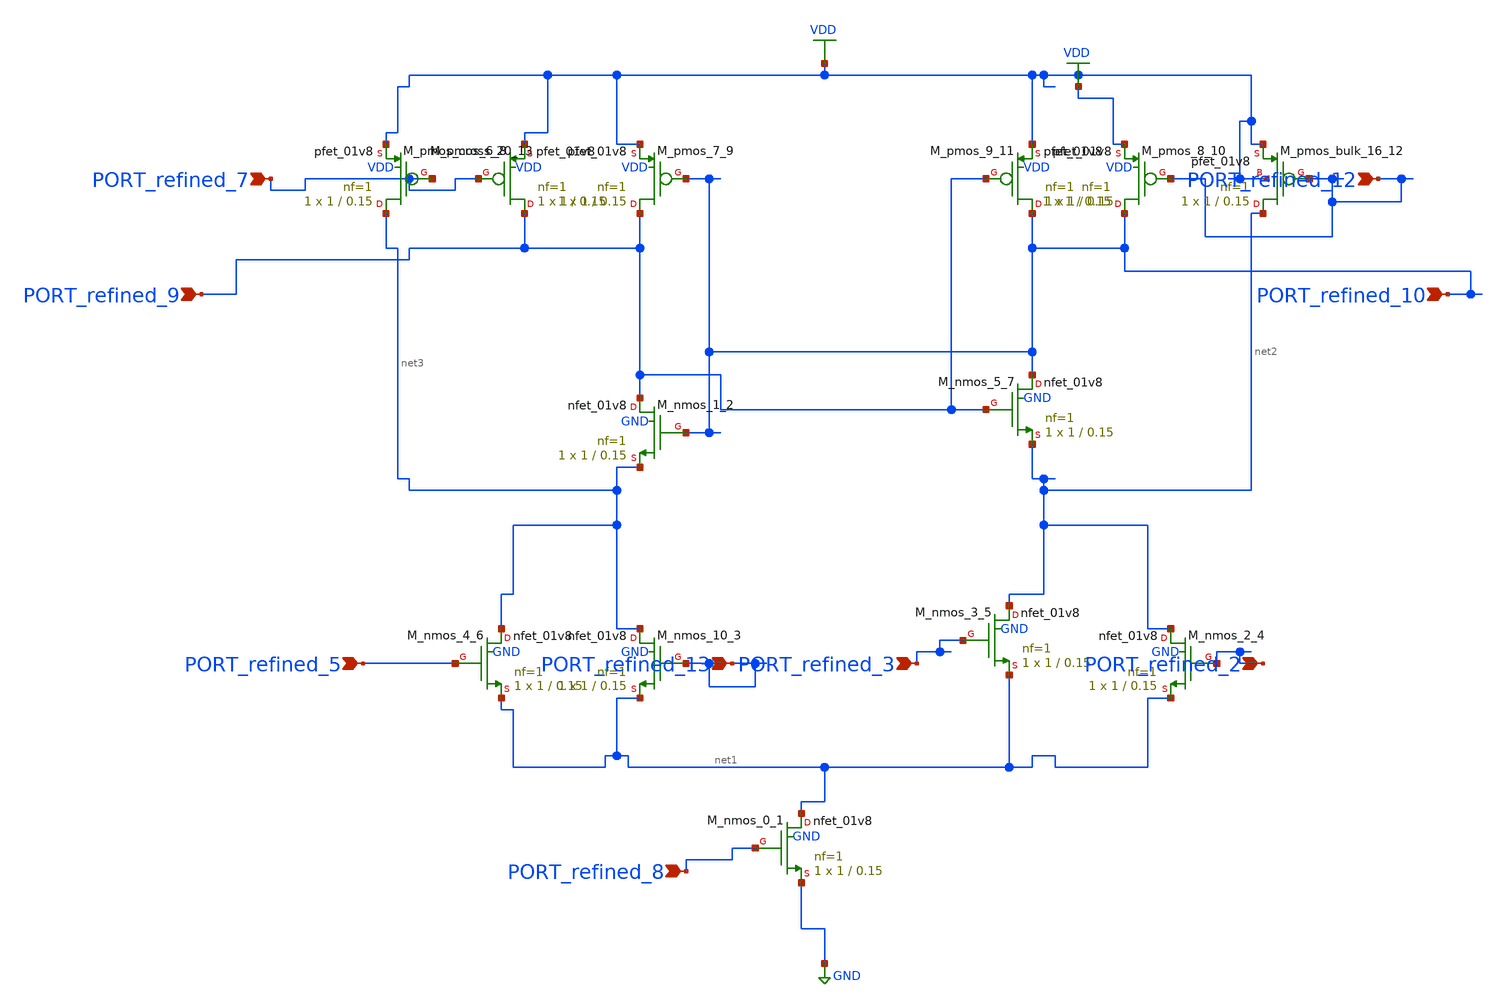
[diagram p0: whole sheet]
** sch_path: schematics/Image2Net/038.sch
**.subckt 038 PORT_refined_9 PORT_refined_10 PORT_refined_5 PORT_refined_2 PORT_refined_3
*+ PORT_refined_8 PORT_refined_7 PORT_refined_13 PORT_refined_12
*.ipin PORT_refined_9
*.ipin PORT_refined_10
*.ipin PORT_refined_5
*.ipin PORT_refined_2
*.ipin PORT_refined_3
*.ipin PORT_refined_8
*.ipin PORT_refined_7
*.ipin PORT_refined_13
*.ipin PORT_refined_12
XM_nmos_0_1 net1 PORT_refined_8 GND GND sky130_fd_pr__nfet_01v8 L=0.15 W=1 nf=1 ad='int((1 + 1)/2) * 1 / 1 * 0.29'
+ as='int((1 + 2)/2) * 1 / 1 * 0.29' pd='2*int((1 + 1)/2) * (1 / 1 + 0.29)' ps='2*int((1 + 2)/2) * (1 / 1 + 0.29)'
+ nrd='0.29 / 1 ' nrs='0.29 / 1 ' sa=0 sb=0 sd=0 mult=1 m=1
XM_nmos_1_2 PORT_refined_9 PORT_refined_10 net3 GND sky130_fd_pr__nfet_01v8 L=0.15 W=1 nf=1 ad='int((1 + 1)/2) * 1 / 1 * 0.29'
+ as='int((1 + 2)/2) * 1 / 1 * 0.29' pd='2*int((1 + 1)/2) * (1 / 1 + 0.29)' ps='2*int((1 + 2)/2) * (1 / 1 + 0.29)'
+ nrd='0.29 / 1 ' nrs='0.29 / 1 ' sa=0 sb=0 sd=0 mult=1 m=1
XM_nmos_10_3 net3 PORT_refined_13 net1 GND sky130_fd_pr__nfet_01v8 L=0.15 W=1 nf=1 ad='int((1 + 1)/2) * 1 / 1 * 0.29'
+ as='int((1 + 2)/2) * 1 / 1 * 0.29' pd='2*int((1 + 1)/2) * (1 / 1 + 0.29)' ps='2*int((1 + 2)/2) * (1 / 1 + 0.29)'
+ nrd='0.29 / 1 ' nrs='0.29 / 1 ' sa=0 sb=0 sd=0 mult=1 m=1
XM_nmos_2_4 net2 PORT_refined_2 net1 GND sky130_fd_pr__nfet_01v8 L=0.15 W=1 nf=1 ad='int((1 + 1)/2) * 1 / 1 * 0.29'
+ as='int((1 + 2)/2) * 1 / 1 * 0.29' pd='2*int((1 + 1)/2) * (1 / 1 + 0.29)' ps='2*int((1 + 2)/2) * (1 / 1 + 0.29)'
+ nrd='0.29 / 1 ' nrs='0.29 / 1 ' sa=0 sb=0 sd=0 mult=1 m=1
XM_nmos_3_5 net2 PORT_refined_3 net1 GND sky130_fd_pr__nfet_01v8 L=0.15 W=1 nf=1 ad='int((1 + 1)/2) * 1 / 1 * 0.29'
+ as='int((1 + 2)/2) * 1 / 1 * 0.29' pd='2*int((1 + 1)/2) * (1 / 1 + 0.29)' ps='2*int((1 + 2)/2) * (1 / 1 + 0.29)'
+ nrd='0.29 / 1 ' nrs='0.29 / 1 ' sa=0 sb=0 sd=0 mult=1 m=1
XM_nmos_4_6 net3 PORT_refined_5 net1 GND sky130_fd_pr__nfet_01v8 L=0.15 W=1 nf=1 ad='int((1 + 1)/2) * 1 / 1 * 0.29'
+ as='int((1 + 2)/2) * 1 / 1 * 0.29' pd='2*int((1 + 1)/2) * (1 / 1 + 0.29)' ps='2*int((1 + 2)/2) * (1 / 1 + 0.29)'
+ nrd='0.29 / 1 ' nrs='0.29 / 1 ' sa=0 sb=0 sd=0 mult=1 m=1
XM_nmos_5_7 PORT_refined_10 PORT_refined_9 net2 GND sky130_fd_pr__nfet_01v8 L=0.15 W=1 nf=1 ad='int((1 + 1)/2) * 1 / 1 * 0.29'
+ as='int((1 + 2)/2) * 1 / 1 * 0.29' pd='2*int((1 + 1)/2) * (1 / 1 + 0.29)' ps='2*int((1 + 2)/2) * (1 / 1 + 0.29)'
+ nrd='0.29 / 1 ' nrs='0.29 / 1 ' sa=0 sb=0 sd=0 mult=1 m=1
XM_pmos_6_8 PORT_refined_9 PORT_refined_7 VDD VDD sky130_fd_pr__pfet_01v8 L=0.15 W=1 nf=1 ad='int((1 + 1)/2) * 1 / 1 * 0.29'
+ as='int((1 + 2)/2) * 1 / 1 * 0.29' pd='2*int((1 + 1)/2) * (1 / 1 + 0.29)' ps='2*int((1 + 2)/2) * (1 / 1 + 0.29)'
+ nrd='0.29 / 1 ' nrs='0.29 / 1 ' sa=0 sb=0 sd=0 mult=1 m=1
XM_pmos_7_9 PORT_refined_9 PORT_refined_10 VDD VDD sky130_fd_pr__pfet_01v8 L=0.15 W=1 nf=1 ad='int((1 + 1)/2) * 1 / 1 * 0.29'
+ as='int((1 + 2)/2) * 1 / 1 * 0.29' pd='2*int((1 + 1)/2) * (1 / 1 + 0.29)' ps='2*int((1 + 2)/2) * (1 / 1 + 0.29)'
+ nrd='0.29 / 1 ' nrs='0.29 / 1 ' sa=0 sb=0 sd=0 mult=1 m=1
XM_pmos_8_10 PORT_refined_10 PORT_refined_12 VDD VDD sky130_fd_pr__pfet_01v8 L=0.15 W=1 nf=1 ad='int((1 + 1)/2) * 1 / 1 * 0.29'
+ as='int((1 + 2)/2) * 1 / 1 * 0.29' pd='2*int((1 + 1)/2) * (1 / 1 + 0.29)' ps='2*int((1 + 2)/2) * (1 / 1 + 0.29)'
+ nrd='0.29 / 1 ' nrs='0.29 / 1 ' sa=0 sb=0 sd=0 mult=1 m=1
XM_pmos_9_11 PORT_refined_10 PORT_refined_9 VDD VDD sky130_fd_pr__pfet_01v8 L=0.15 W=1 nf=1 ad='int((1 + 1)/2) * 1 / 1 * 0.29'
+ as='int((1 + 2)/2) * 1 / 1 * 0.29' pd='2*int((1 + 1)/2) * (1 / 1 + 0.29)' ps='2*int((1 + 2)/2) * (1 / 1 + 0.29)'
+ nrd='0.29 / 1 ' nrs='0.29 / 1 ' sa=0 sb=0 sd=0 mult=1 m=1
XM_pmos_bulk_16_12 net2 PORT_refined_12 VDD VDD sky130_fd_pr__pfet_01v8 L=0.15 W=1 nf=1 ad='int((1 + 1)/2) * 1 / 1 * 0.29'
+ as='int((1 + 2)/2) * 1 / 1 * 0.29' pd='2*int((1 + 1)/2) * (1 / 1 + 0.29)' ps='2*int((1 + 2)/2) * (1 / 1 + 0.29)'
+ nrd='0.29 / 1 ' nrs='0.29 / 1 ' sa=0 sb=0 sd=0 mult=1 m=1
XM_pmos_cross_20_13 net3 PORT_refined_7 VDD VDD sky130_fd_pr__pfet_01v8 L=0.15 W=1 nf=1 ad='int((1 + 1)/2) * 1 / 1 * 0.29'
+ as='int((1 + 2)/2) * 1 / 1 * 0.29' pd='2*int((1 + 1)/2) * (1 / 1 + 0.29)' ps='2*int((1 + 2)/2) * (1 / 1 + 0.29)'
+ nrd='0.29 / 1 ' nrs='0.29 / 1 ' sa=0 sb=0 sd=0 mult=1 m=1
**.ends
.GLOBAL GND
.GLOBAL VDD
.end
